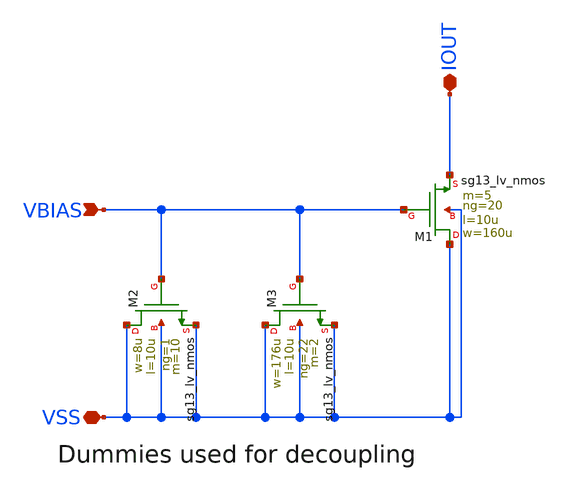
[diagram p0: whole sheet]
** sch_path: JKU_TC1/design_data/sfl-test-cells/xschem/tailsrcs/tail_src_n.sch
**.subckt tail_src_n VBIAS VSS IOUT
*.ipin VBIAS
*.iopin VSS
*.iopin IOUT
XM1 VSS VBIAS IOUT VSS sg13_lv_nmos w=160u l=10u ng=20 m=5 mm_ok=1
XM2 VSS VBIAS VSS VSS sg13_lv_nmos w=8u l=10u ng=1 m=10 mm_ok=1
XM3 VSS VBIAS VSS VSS sg13_lv_nmos w=176u l=10u ng=22 m=2 mm_ok=1
**.ends
.end
